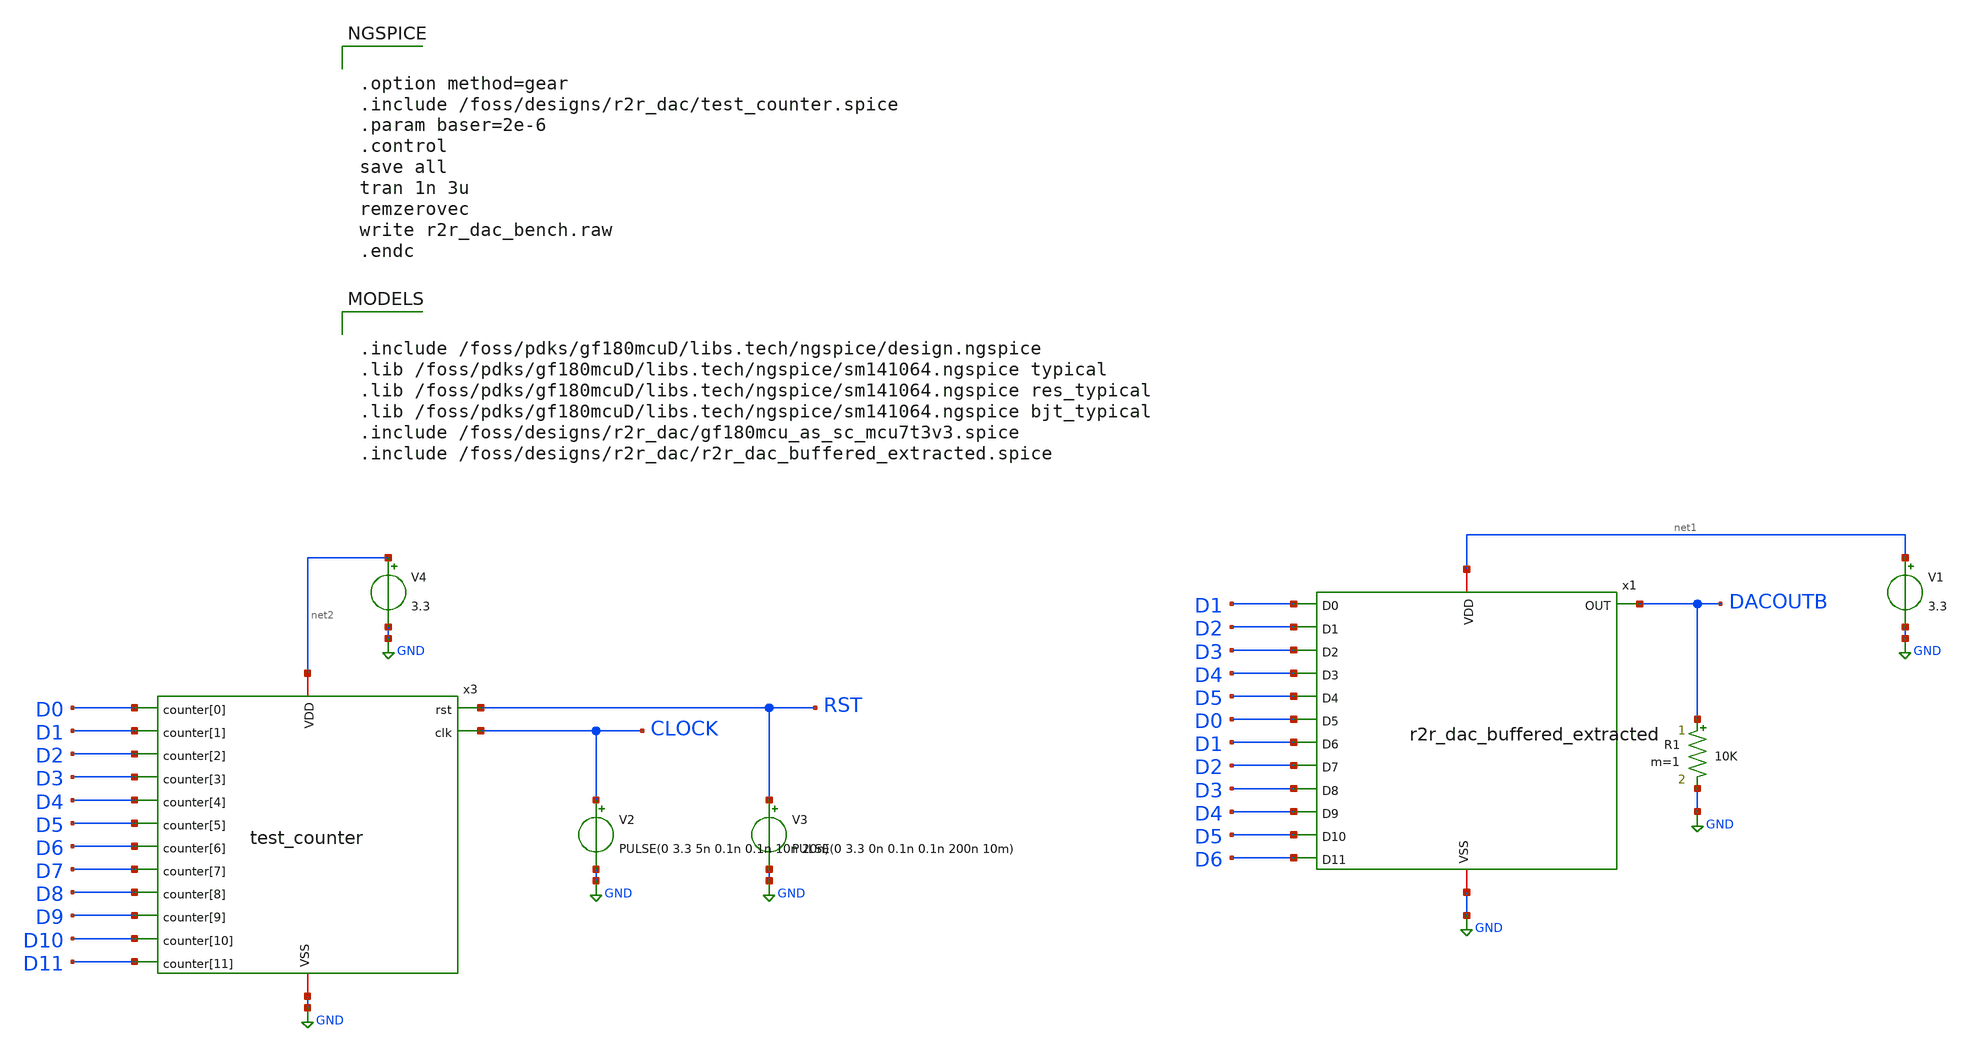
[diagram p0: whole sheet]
** sch_path: macros/Analog/r2r_dac/r2r_dac_bench.sch
**.subckt r2r_dac_bench
V1 net1 GND 3.3
V2 CLOCK GND PULSE(0 3.3 5n 0.1n 0.1n 10n 20n)
V3 RST GND PULSE(0 3.3 0n 0.1n 0.1n 200n 10m)
x3 net2 GND CLOCK D0 D10 D11 D1 D2 D3 D4 D5 D6 D7 D8 D9 RST test_counter
R1 DACOUTB GND 10K m=1
V4 net2 GND 3.3
x1 net1 GND D1 D2 D3 D4 D5 D0 D1 D2 D3 D4 D5 D6 DACOUTB r2r_dac_buffered_extracted
**** begin user architecture code

.include /foss/pdks/gf180mcuD/libs.tech/ngspice/design.ngspice
.lib /foss/pdks/gf180mcuD/libs.tech/ngspice/sm141064.ngspice typical
.lib /foss/pdks/gf180mcuD/libs.tech/ngspice/sm141064.ngspice res_typical
.lib /foss/pdks/gf180mcuD/libs.tech/ngspice/sm141064.ngspice bjt_typical
.include /foss/designs/r2r_dac/gf180mcu_as_sc_mcu7t3v3.spice
.include /foss/designs/r2r_dac/r2r_dac_buffered_extracted.spice



.option method=gear
.include /foss/designs/r2r_dac/test_counter.spice
.param baser=2e-6
.control
save all
tran 1n 3u
remzerovec
write r2r_dac_bench.raw
.endc


**** end user architecture code
**.ends
.GLOBAL GND
.end
